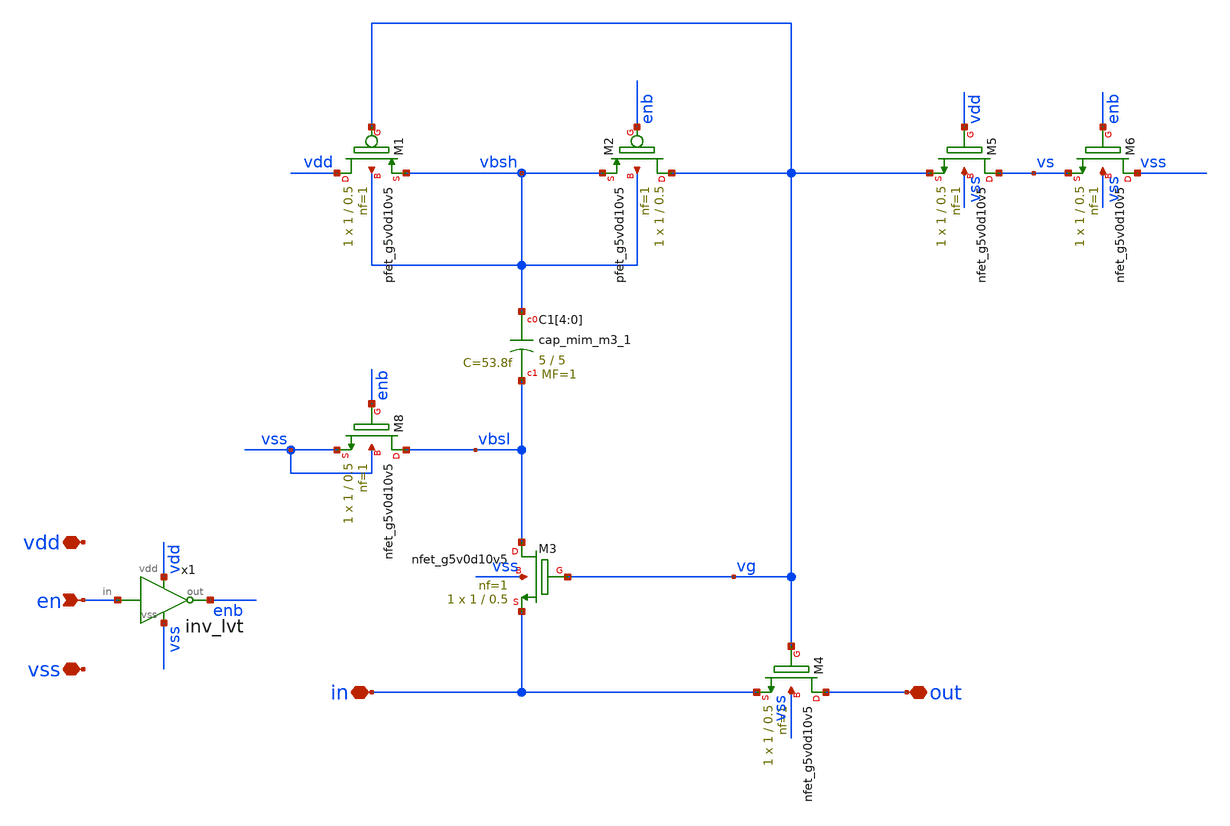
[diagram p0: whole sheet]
** sch_path: xschem/adc/bootstrapped_sw_hv.sch
**.subckt bootstrapped_sw_hv in out vdd vss en
*.iopin in
*.iopin out
*.iopin vdd
*.iopin vss
*.ipin en
XM1 vdd vg vbsh vbsh sky130_fd_pr__pfet_g5v0d10v5 L=0.5 W=1 nf=1 ad='int((nf+1)/2) * W/nf * 0.29' as='int((nf+2)/2) * W/nf * 0.29'
+ pd='2*int((nf+1)/2) * (W/nf + 0.29)' ps='2*int((nf+2)/2) * (W/nf + 0.29)' nrd='0.29 / W' nrs='0.29 / W'
+ sa=0 sb=0 sd=0 mult=1 m=1
XM2 vg enb vbsh vbsh sky130_fd_pr__pfet_g5v0d10v5 L=0.5 W=1 nf=1 ad='int((nf+1)/2) * W/nf * 0.29' as='int((nf+2)/2) * W/nf * 0.29'
+ pd='2*int((nf+1)/2) * (W/nf + 0.29)' ps='2*int((nf+2)/2) * (W/nf + 0.29)' nrd='0.29 / W' nrs='0.29 / W'
+ sa=0 sb=0 sd=0 mult=1 m=1
XC1[4] vbsh vbsl sky130_fd_pr__cap_mim_m3_1 W=5 L=5 MF=1 m=1
XC1[3] vbsh vbsl sky130_fd_pr__cap_mim_m3_1 W=5 L=5 MF=1 m=1
XC1[2] vbsh vbsl sky130_fd_pr__cap_mim_m3_1 W=5 L=5 MF=1 m=1
XC1[1] vbsh vbsl sky130_fd_pr__cap_mim_m3_1 W=5 L=5 MF=1 m=1
XC1[0] vbsh vbsl sky130_fd_pr__cap_mim_m3_1 W=5 L=5 MF=1 m=1
XM8 vbsl enb vss vss sky130_fd_pr__nfet_g5v0d10v5 L=0.5 W=1 nf=1 ad='int((nf+1)/2) * W/nf * 0.29' as='int((nf+2)/2) * W/nf * 0.29'
+ pd='2*int((nf+1)/2) * (W/nf + 0.29)' ps='2*int((nf+2)/2) * (W/nf + 0.29)' nrd='0.29 / W' nrs='0.29 / W'
+ sa=0 sb=0 sd=0 mult=1 m=1
XM3 vbsl vg in vss sky130_fd_pr__nfet_g5v0d10v5 L=0.5 W=1 nf=1 ad='int((nf+1)/2) * W/nf * 0.29' as='int((nf+2)/2) * W/nf * 0.29'
+ pd='2*int((nf+1)/2) * (W/nf + 0.29)' ps='2*int((nf+2)/2) * (W/nf + 0.29)' nrd='0.29 / W' nrs='0.29 / W'
+ sa=0 sb=0 sd=0 mult=1 m=1
XM4 out vg in vss sky130_fd_pr__nfet_g5v0d10v5 L=0.5 W=1 nf=1 ad='int((nf+1)/2) * W/nf * 0.29' as='int((nf+2)/2) * W/nf * 0.29'
+ pd='2*int((nf+1)/2) * (W/nf + 0.29)' ps='2*int((nf+2)/2) * (W/nf + 0.29)' nrd='0.29 / W' nrs='0.29 / W'
+ sa=0 sb=0 sd=0 mult=1 m=1
XM5 vs vdd vg vss sky130_fd_pr__nfet_g5v0d10v5 L=0.5 W=1 nf=1 ad='int((nf+1)/2) * W/nf * 0.29' as='int((nf+2)/2) * W/nf * 0.29'
+ pd='2*int((nf+1)/2) * (W/nf + 0.29)' ps='2*int((nf+2)/2) * (W/nf + 0.29)' nrd='0.29 / W' nrs='0.29 / W'
+ sa=0 sb=0 sd=0 mult=1 m=1
XM6 vss enb vs vss sky130_fd_pr__nfet_g5v0d10v5 L=0.5 W=1 nf=1 ad='int((nf+1)/2) * W/nf * 0.29' as='int((nf+2)/2) * W/nf * 0.29'
+ pd='2*int((nf+1)/2) * (W/nf + 0.29)' ps='2*int((nf+2)/2) * (W/nf + 0.29)' nrd='0.29 / W' nrs='0.29 / W'
+ sa=0 sb=0 sd=0 mult=1 m=1
x1 vdd en enb vss inv_lvt
**.ends
.end
